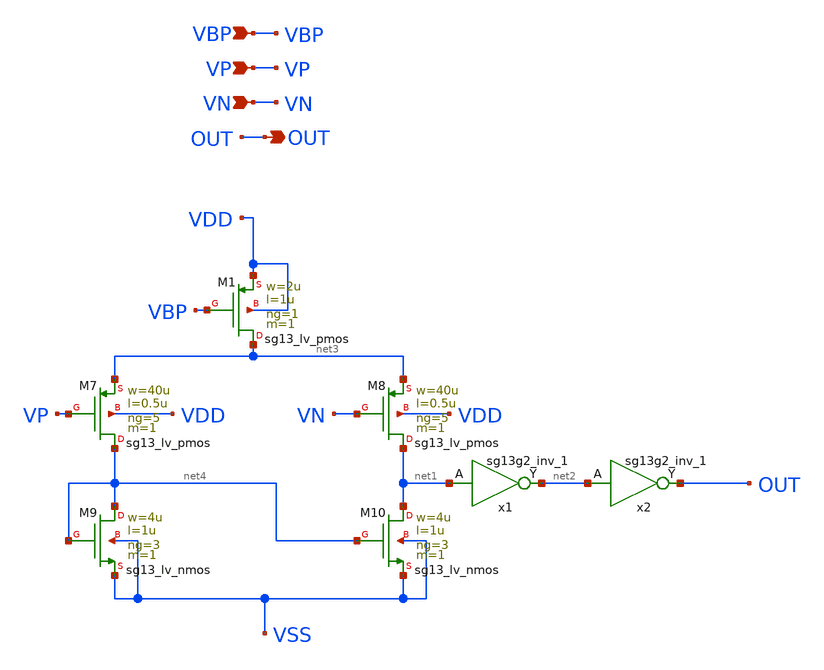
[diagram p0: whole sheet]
** sch_path: design/blocks/comparator/schematic/comp_inf.sch
**.subckt comp_inf OUT VN VP VBP
*.opin OUT
*.ipin VN
*.ipin VP
*.ipin VBP
x1 net2 net1 VDD VSS sg13g2_inv_1
x2 OUT net2 VDD VSS sg13g2_inv_1
XM1 net3 VBP VDD VDD sg13_lv_pmos w=2u l=1u ng=1 m=1 mm_ok=1
XM7 net4 VP net3 VDD sg13_lv_pmos w=40u l=0.5u ng=5 m=1 mm_ok=1
XM8 net1 VN net3 VDD sg13_lv_pmos w=40u l=0.5u ng=5 m=1 mm_ok=1
XM9 net4 net4 VSS VSS sg13_lv_nmos w=4u l=1u ng=3 m=1 mm_ok=1
XM10 net1 net4 VSS VSS sg13_lv_nmos w=4u l=1u ng=3 m=1 mm_ok=1
**.ends

* expanding   symbol:  sg13g2_inv_1.sym # of pins=2
** sym_path: sg13g2_inv_1.sym
** sch_path: sg13g2_inv_1.sch
.subckt sg13g2_inv_1 Y A VDD VSS
*.opin Y
*.ipin A
*.iopin VDD
*.iopin VSS
XM1 Y A VSS VSS sg13_lv_nmos w=740.00n l=130.00n ng=1 m=1 mm_ok=1
XM2 Y A VDD VDD sg13_lv_pmos w=1.12u l=130.00n ng=1 m=1 mm_ok=1
.ends

.end
